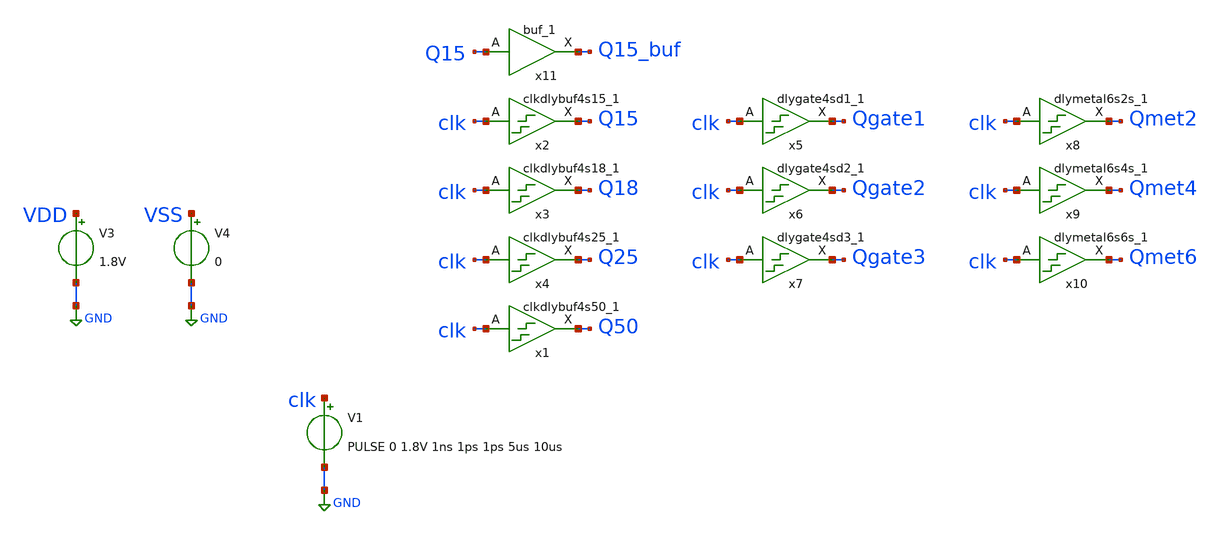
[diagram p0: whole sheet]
** sch_path: xschem/tests/dummy_tests/dummy_clkdly_test.sch
**.subckt dummy_clkdly_test
V3 VDD GND 1.8V
V4 VSS GND 0
x1 clk VSS VSS VDD VDD Q50 sky130_fd_sc_hd__clkdlybuf4s50_1
V1 clk GND PULSE 0 1.8V 1ns 1ps 1ps 5us 10us
x2 clk VSS VSS VDD VDD Q15 sky130_fd_sc_hd__clkdlybuf4s15_1
x3 clk VSS VSS VDD VDD Q18 sky130_fd_sc_hd__clkdlybuf4s18_1
x4 clk VSS VSS VDD VDD Q25 sky130_fd_sc_hd__clkdlybuf4s25_1
x5 clk VSS VSS VDD VDD Qgate1 sky130_fd_sc_hd__dlygate4sd1_1
x6 clk VSS VSS VDD VDD Qgate2 sky130_fd_sc_hd__dlygate4sd2_1
x7 clk VSS VSS VDD VDD Qgate3 sky130_fd_sc_hd__dlygate4sd3_1
x8 clk VSS VSS VDD VDD Qmet2 sky130_fd_sc_hd__dlymetal6s2s_1
x9 clk VSS VSS VDD VDD Qmet4 sky130_fd_sc_hd__dlymetal6s4s_1
x10 clk VSS VSS VDD VDD Qmet6 sky130_fd_sc_hd__dlymetal6s6s_1
x11 Q15 VSS VSS VDD VDD Q15_buf sky130_fd_sc_hd__buf_1
**** begin user architecture code
 .lib $::SKYWATER_MODELS/sky130.lib.spice tt
.include $::SKYWATER_STDCELLS/sky130_fd_sc_hd.spice


.options acct list
.temp 25
*vvcc VDD 0 dc 1.8
*vvss VSS 0 0
.control
tran 0.005n 3n
*dc v1 0 1.8V 0.1
*plot RST_PLS clk+2 Pulse+4
plot clk Q50 clk+2 Q25+2 clk=4 Q18+4 clk+6 Q15+6 Q15_buf+8
plot clk Qgate3 clk+2 Qgate2+2 clk+4 Qgate1+4
plot clk Qmet6 clk+2 Qmet4+2 clk+4 Qmet2+4
write dummy_clkdly_test.raw
.endc


**** end user architecture code
**.ends
.GLOBAL GND
.end
